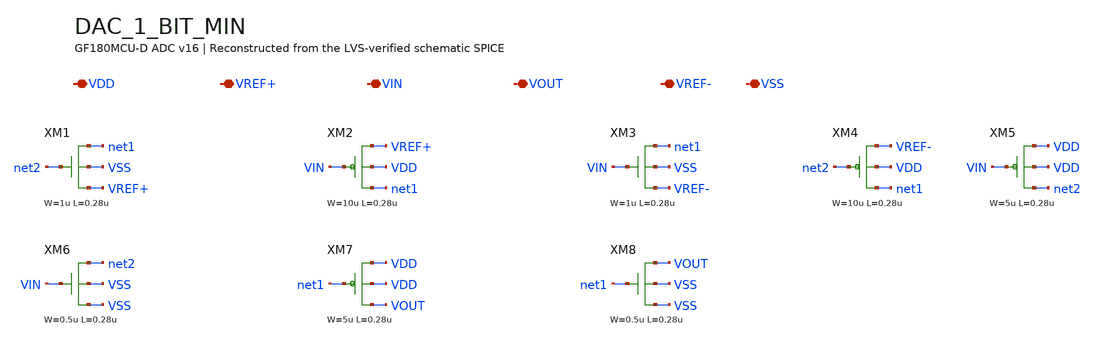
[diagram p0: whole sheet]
** sch_path: src/schematics/INTEGRATION/ADC_final/ADC_v17_Xschem/DAC_1_BIT_MIN.sch
* Copyright (C) 1998-2026 Stefan Frederik Schippers
* This program is free software; you can redistribute it and/or modify
* it under the terms of the GNU General Public License as published by
* the Free Software Foundation; either version 2 of the License, or
* (at your option) any later version.
**.subckt DAC_1_BIT_MIN VDD VREF+ VIN VOUT VREF- VSS
*.iopin VDD
*.iopin VREF+
*.iopin VIN
*.iopin VOUT
*.iopin VREF-
*.iopin VSS
XM1 net1 net2 VREF+ VSS nfet_03v3 L=0.28u W=1u nf=2 ad='int((nf+1)/2) * W/nf * 0.18u' as='int((nf+2)/2) * W/nf * 0.18u'
+ pd='2*int((nf+1)/2) * (W/nf + 0.18u)' ps='2*int((nf+2)/2) * (W/nf + 0.18u)' nrd='0.18u / W' nrs='0.18u / W'
+ sa=0 sb=0 sd=0
XM2 net1 VIN VREF+ VDD pfet_03v3 L=0.28u W=10u nf=2 ad='int((nf+1)/2) * W/nf * 0.18u' as='int((nf+2)/2) * W/nf * 0.18u'
+ pd='2*int((nf+1)/2) * (W/nf + 0.18u)' ps='2*int((nf+2)/2) * (W/nf + 0.18u)' nrd='0.18u / W' nrs='0.18u / W'
+ sa=0 sb=0 sd=0
XM3 net1 VIN VREF- VSS nfet_03v3 L=0.28u W=1u nf=2 ad='int((nf+1)/2) * W/nf * 0.18u' as='int((nf+2)/2) * W/nf * 0.18u'
+ pd='2*int((nf+1)/2) * (W/nf + 0.18u)' ps='2*int((nf+2)/2) * (W/nf + 0.18u)' nrd='0.18u / W' nrs='0.18u / W'
+ sa=0 sb=0 sd=0
XM4 net1 net2 VREF- VDD pfet_03v3 L=0.28u W=10u nf=2 ad='int((nf+1)/2) * W/nf * 0.18u' as='int((nf+2)/2) * W/nf * 0.18u'
+ pd='2*int((nf+1)/2) * (W/nf + 0.18u)' ps='2*int((nf+2)/2) * (W/nf + 0.18u)' nrd='0.18u / W' nrs='0.18u / W'
+ sa=0 sb=0 sd=0
XM5 net2 VIN VDD VDD pfet_03v3 L=0.28u W=5u nf=1 ad='int((nf+1)/2) * W/nf * 0.18u' as='int((nf+2)/2) * W/nf * 0.18u'
+ pd='2*int((nf+1)/2) * (W/nf + 0.18u)' ps='2*int((nf+2)/2) * (W/nf + 0.18u)' nrd='0.18u / W' nrs='0.18u / W'
+ sa=0 sb=0 sd=0
XM6 net2 VIN VSS VSS nfet_03v3 L=0.28u W=0.5u nf=1 ad='int((nf+1)/2) * W/nf * 0.18u' as='int((nf+2)/2) * W/nf * 0.18u'
+ pd='2*int((nf+1)/2) * (W/nf + 0.18u)' ps='2*int((nf+2)/2) * (W/nf + 0.18u)' nrd='0.18u / W' nrs='0.18u / W'
+ sa=0 sb=0 sd=0
XM7 VOUT net1 VDD VDD pfet_03v3 L=0.28u W=5u nf=1 ad='int((nf+1)/2) * W/nf * 0.18u' as='int((nf+2)/2) * W/nf * 0.18u'
+ pd='2*int((nf+1)/2) * (W/nf + 0.18u)' ps='2*int((nf+2)/2) * (W/nf + 0.18u)' nrd='0.18u / W' nrs='0.18u / W'
+ sa=0 sb=0 sd=0
XM8 VOUT net1 VSS VSS nfet_03v3 L=0.28u W=0.5u nf=1 ad='int((nf+1)/2) * W/nf * 0.18u' as='int((nf+2)/2) * W/nf * 0.18u'
+ pd='2*int((nf+1)/2) * (W/nf + 0.18u)' ps='2*int((nf+2)/2) * (W/nf + 0.18u)' nrd='0.18u / W' nrs='0.18u / W'
+ sa=0 sb=0 sd=0
**.ends
.end
